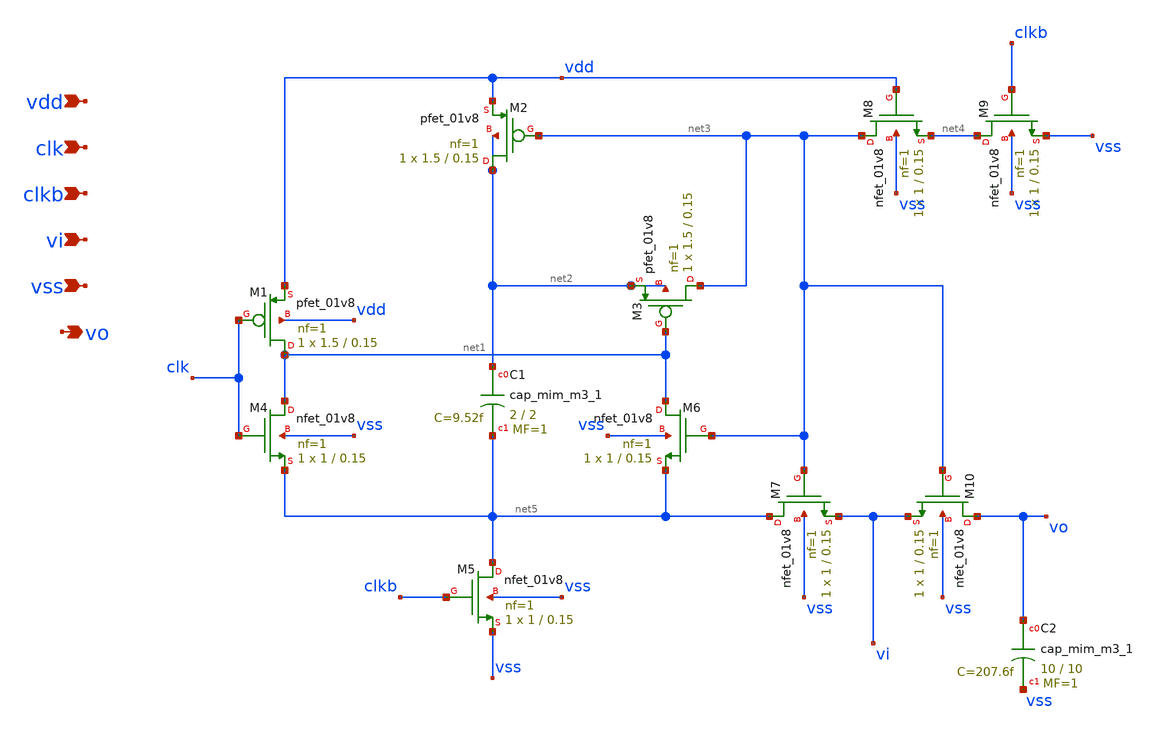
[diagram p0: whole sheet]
** sch_path: xschem/bsw.sch
**.subckt bsw vdd clk clkb vi vss vo
*.ipin vdd
*.ipin clk
*.ipin clkb
*.ipin vi
*.ipin vss
*.opin vo
XM1 net1 clk vdd vdd sky130_fd_pr__pfet_01v8 L=0.15 W=1.5 nf=1 ad='int((nf+1)/2) * W/nf * 0.29' as='int((nf+2)/2) * W/nf * 0.29'
+ pd='2*int((nf+1)/2) * (W/nf + 0.29)' ps='2*int((nf+2)/2) * (W/nf + 0.29)' nrd='0.29 / W' nrs='0.29 / W'
+ sa=0 sb=0 sd=0 mult=1 m=1
XM2 net2 net3 vdd net2 sky130_fd_pr__pfet_01v8 L=0.15 W=1.5 nf=1 ad='int((nf+1)/2) * W/nf * 0.29' as='int((nf+2)/2) * W/nf * 0.29'
+ pd='2*int((nf+1)/2) * (W/nf + 0.29)' ps='2*int((nf+2)/2) * (W/nf + 0.29)' nrd='0.29 / W' nrs='0.29 / W'
+ sa=0 sb=0 sd=0 mult=1 m=1
XM3 net3 net1 net2 net2 sky130_fd_pr__pfet_01v8 L=0.15 W=1.5 nf=1 ad='int((nf+1)/2) * W/nf * 0.29' as='int((nf+2)/2) * W/nf * 0.29'
+ pd='2*int((nf+1)/2) * (W/nf + 0.29)' ps='2*int((nf+2)/2) * (W/nf + 0.29)' nrd='0.29 / W' nrs='0.29 / W'
+ sa=0 sb=0 sd=0 mult=1 m=1
XM4 net1 clk net5 vss sky130_fd_pr__nfet_01v8 L=0.15 W=1 nf=1 ad='int((nf+1)/2) * W/nf * 0.29' as='int((nf+2)/2) * W/nf * 0.29'
+ pd='2*int((nf+1)/2) * (W/nf + 0.29)' ps='2*int((nf+2)/2) * (W/nf + 0.29)' nrd='0.29 / W' nrs='0.29 / W'
+ sa=0 sb=0 sd=0 mult=1 m=1
XM5 net5 clkb vss vss sky130_fd_pr__nfet_01v8 L=0.15 W=1 nf=1 ad='int((nf+1)/2) * W/nf * 0.29' as='int((nf+2)/2) * W/nf * 0.29'
+ pd='2*int((nf+1)/2) * (W/nf + 0.29)' ps='2*int((nf+2)/2) * (W/nf + 0.29)' nrd='0.29 / W' nrs='0.29 / W'
+ sa=0 sb=0 sd=0 mult=1 m=1
XM6 net1 net3 net5 vss sky130_fd_pr__nfet_01v8 L=0.15 W=1 nf=1 ad='int((nf+1)/2) * W/nf * 0.29' as='int((nf+2)/2) * W/nf * 0.29'
+ pd='2*int((nf+1)/2) * (W/nf + 0.29)' ps='2*int((nf+2)/2) * (W/nf + 0.29)' nrd='0.29 / W' nrs='0.29 / W'
+ sa=0 sb=0 sd=0 mult=1 m=1
XM7 net5 net3 vi vss sky130_fd_pr__nfet_01v8 L=0.15 W=1 nf=1 ad='int((nf+1)/2) * W/nf * 0.29' as='int((nf+2)/2) * W/nf * 0.29'
+ pd='2*int((nf+1)/2) * (W/nf + 0.29)' ps='2*int((nf+2)/2) * (W/nf + 0.29)' nrd='0.29 / W' nrs='0.29 / W'
+ sa=0 sb=0 sd=0 mult=1 m=1
XM8 net3 vdd net4 vss sky130_fd_pr__nfet_01v8 L=0.15 W=1 nf=1 ad='int((nf+1)/2) * W/nf * 0.29' as='int((nf+2)/2) * W/nf * 0.29'
+ pd='2*int((nf+1)/2) * (W/nf + 0.29)' ps='2*int((nf+2)/2) * (W/nf + 0.29)' nrd='0.29 / W' nrs='0.29 / W'
+ sa=0 sb=0 sd=0 mult=1 m=1
XM9 net4 clkb vss vss sky130_fd_pr__nfet_01v8 L=0.15 W=1 nf=1 ad='int((nf+1)/2) * W/nf * 0.29' as='int((nf+2)/2) * W/nf * 0.29'
+ pd='2*int((nf+1)/2) * (W/nf + 0.29)' ps='2*int((nf+2)/2) * (W/nf + 0.29)' nrd='0.29 / W' nrs='0.29 / W'
+ sa=0 sb=0 sd=0 mult=1 m=1
XC1 net2 net5 sky130_fd_pr__cap_mim_m3_1 W=2 L=2 MF=1 m=1
XM10 vo net3 vi vss sky130_fd_pr__nfet_01v8 L=0.15 W=1 nf=1 ad='int((nf+1)/2) * W/nf * 0.29' as='int((nf+2)/2) * W/nf * 0.29'
+ pd='2*int((nf+1)/2) * (W/nf + 0.29)' ps='2*int((nf+2)/2) * (W/nf + 0.29)' nrd='0.29 / W' nrs='0.29 / W'
+ sa=0 sb=0 sd=0 mult=1 m=1
XC2 vo vss sky130_fd_pr__cap_mim_m3_1 W=10 L=10 MF=1 m=1
**.ends
.end
